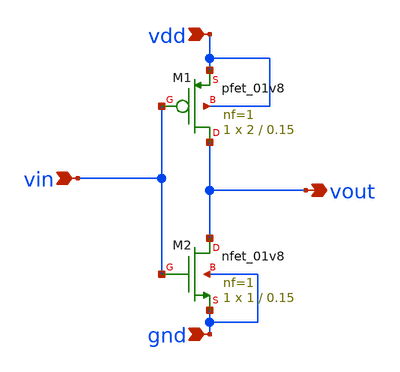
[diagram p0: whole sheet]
** sch_path: Xschem files/inver_vtc.sch
**.subckt inver_vtc vin gnd vdd vout
*.ipin vin
*.ipin gnd
*.ipin vdd
*.opin vout
XM1 vout vin vdd vdd sky130_fd_pr__pfet_01v8 L=0.15 W=2 nf=1 ad='int((nf+1)/2) * W/nf * 0.29' as='int((nf+2)/2) * W/nf * 0.29'
+ pd='2*int((nf+1)/2) * (W/nf + 0.29)' ps='2*int((nf+2)/2) * (W/nf + 0.29)' nrd='0.29 / W' nrs='0.29 / W'
+ sa=0 sb=0 sd=0 mult=1 m=1
XM2 vout vin gnd gnd sky130_fd_pr__nfet_01v8 L=0.15 W=1 nf=1 ad='int((nf+1)/2) * W/nf * 0.29' as='int((nf+2)/2) * W/nf * 0.29'
+ pd='2*int((nf+1)/2) * (W/nf + 0.29)' ps='2*int((nf+2)/2) * (W/nf + 0.29)' nrd='0.29 / W' nrs='0.29 / W'
+ sa=0 sb=0 sd=0 mult=1 m=1
**.ends
.end
